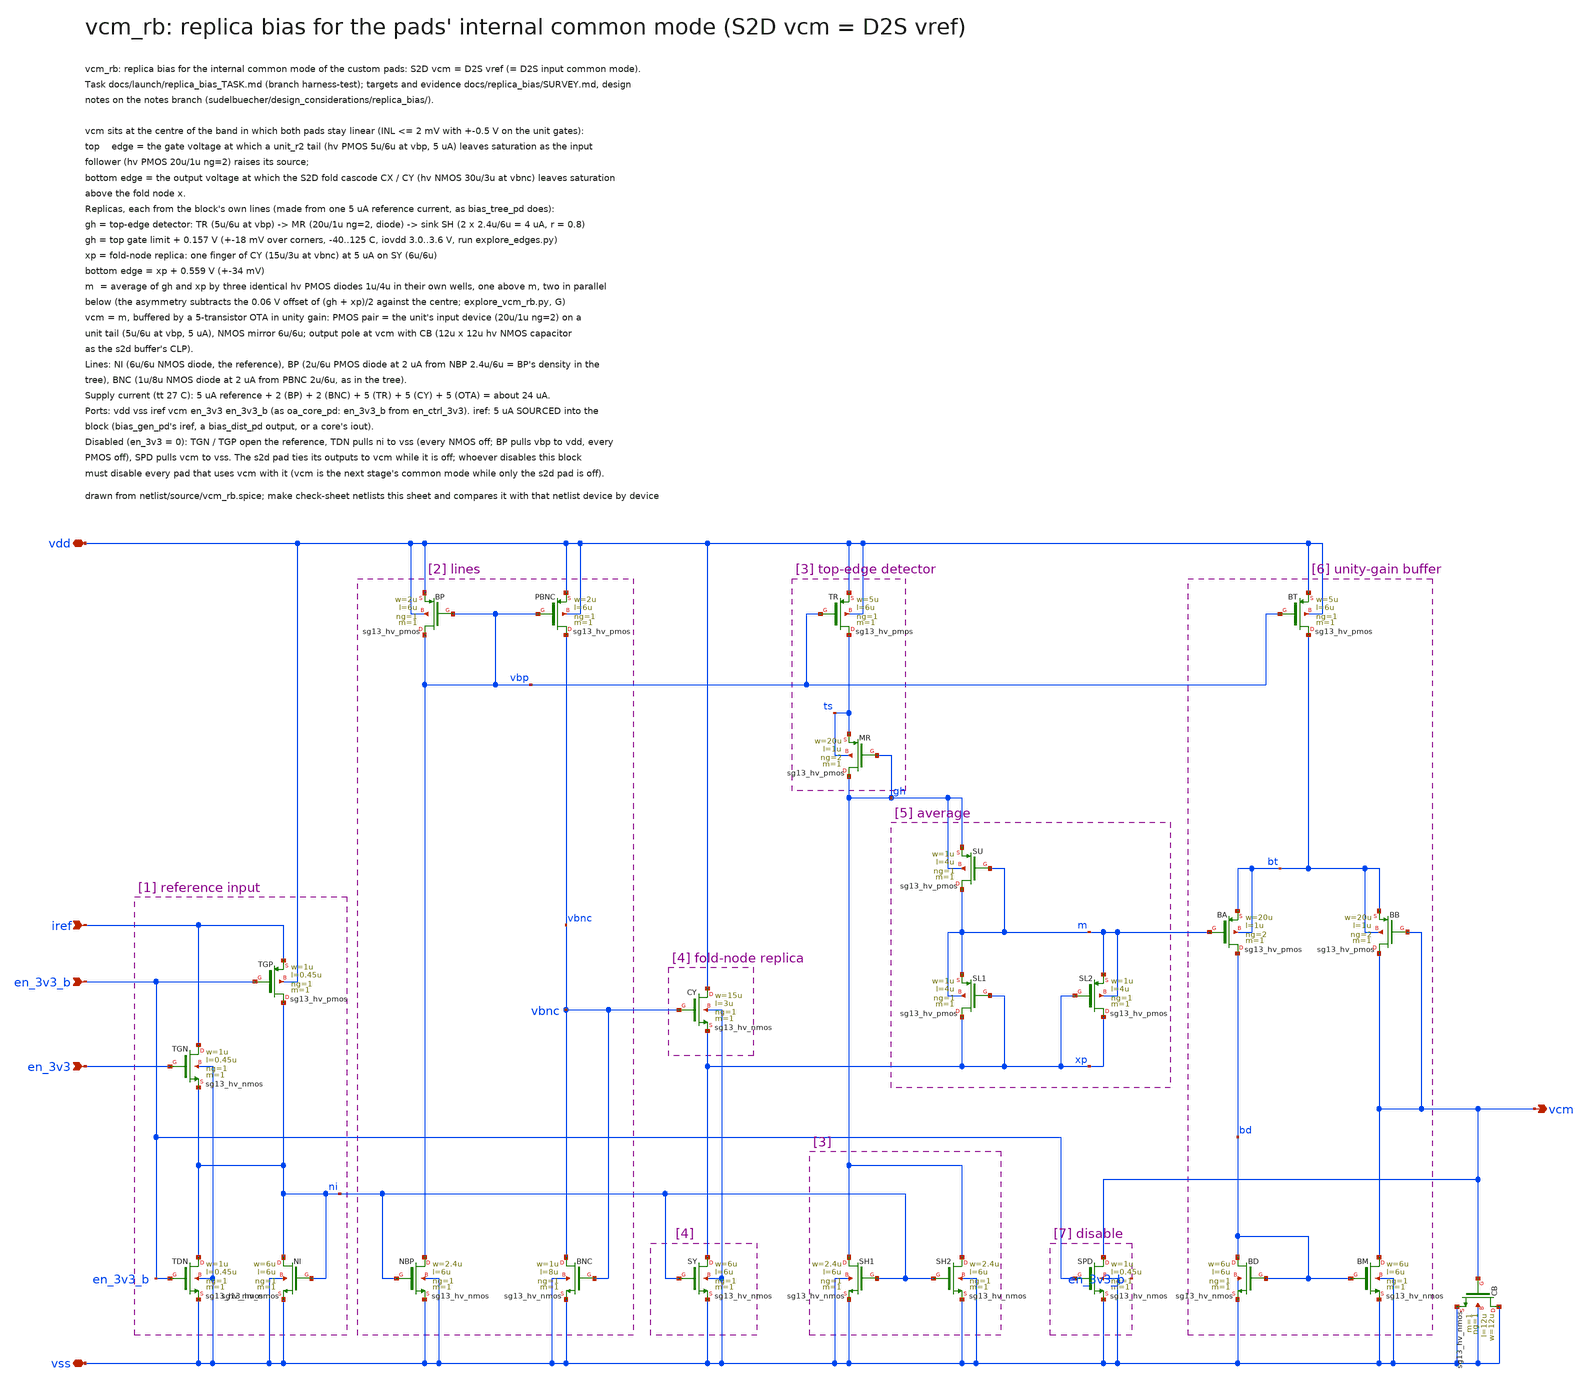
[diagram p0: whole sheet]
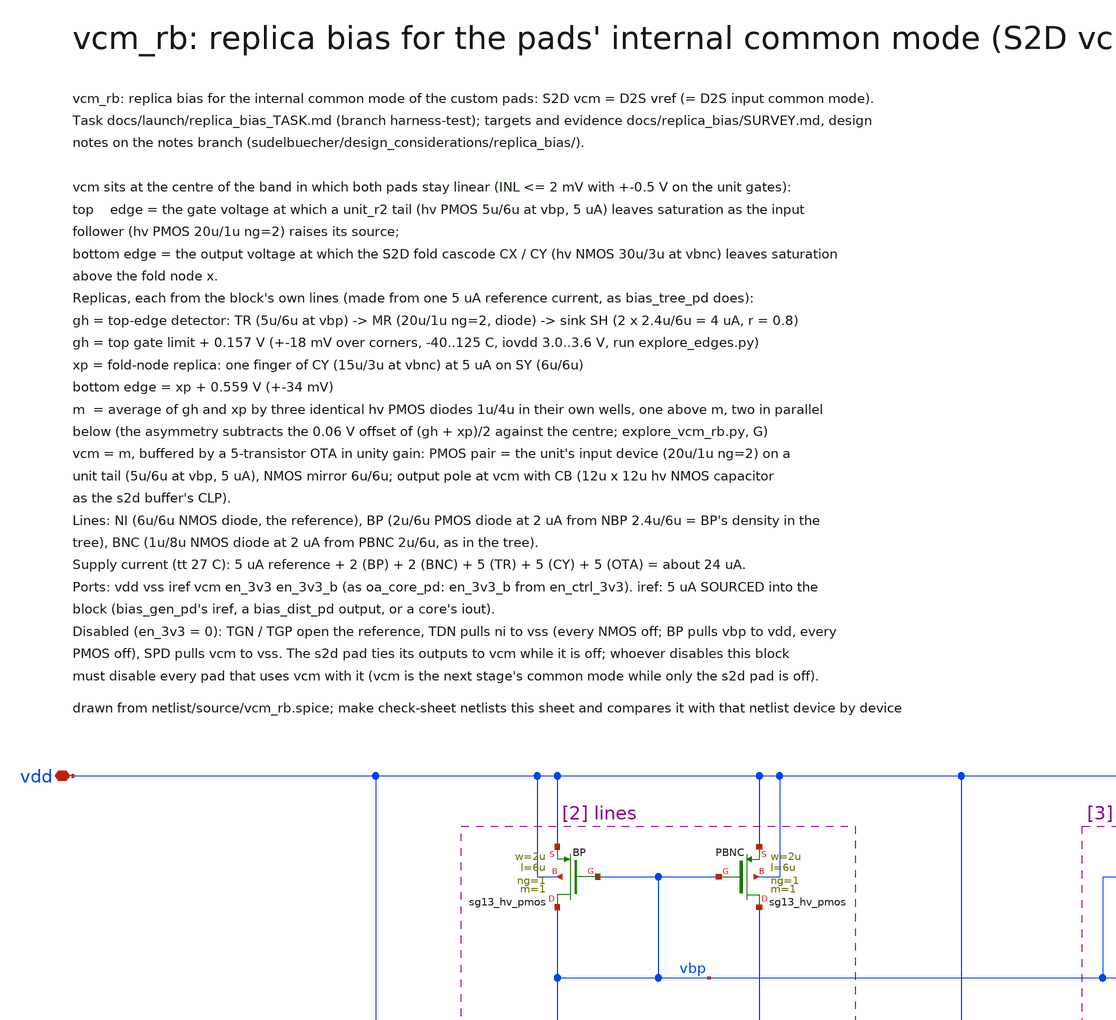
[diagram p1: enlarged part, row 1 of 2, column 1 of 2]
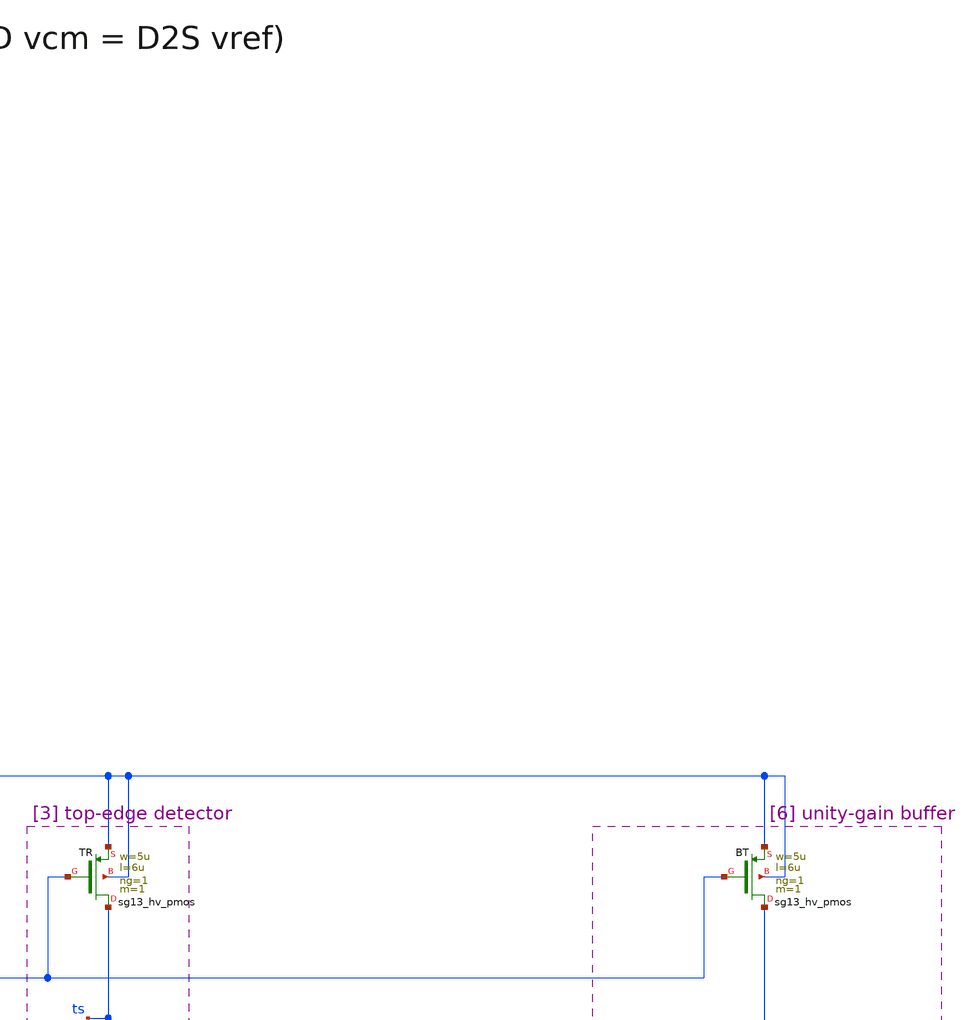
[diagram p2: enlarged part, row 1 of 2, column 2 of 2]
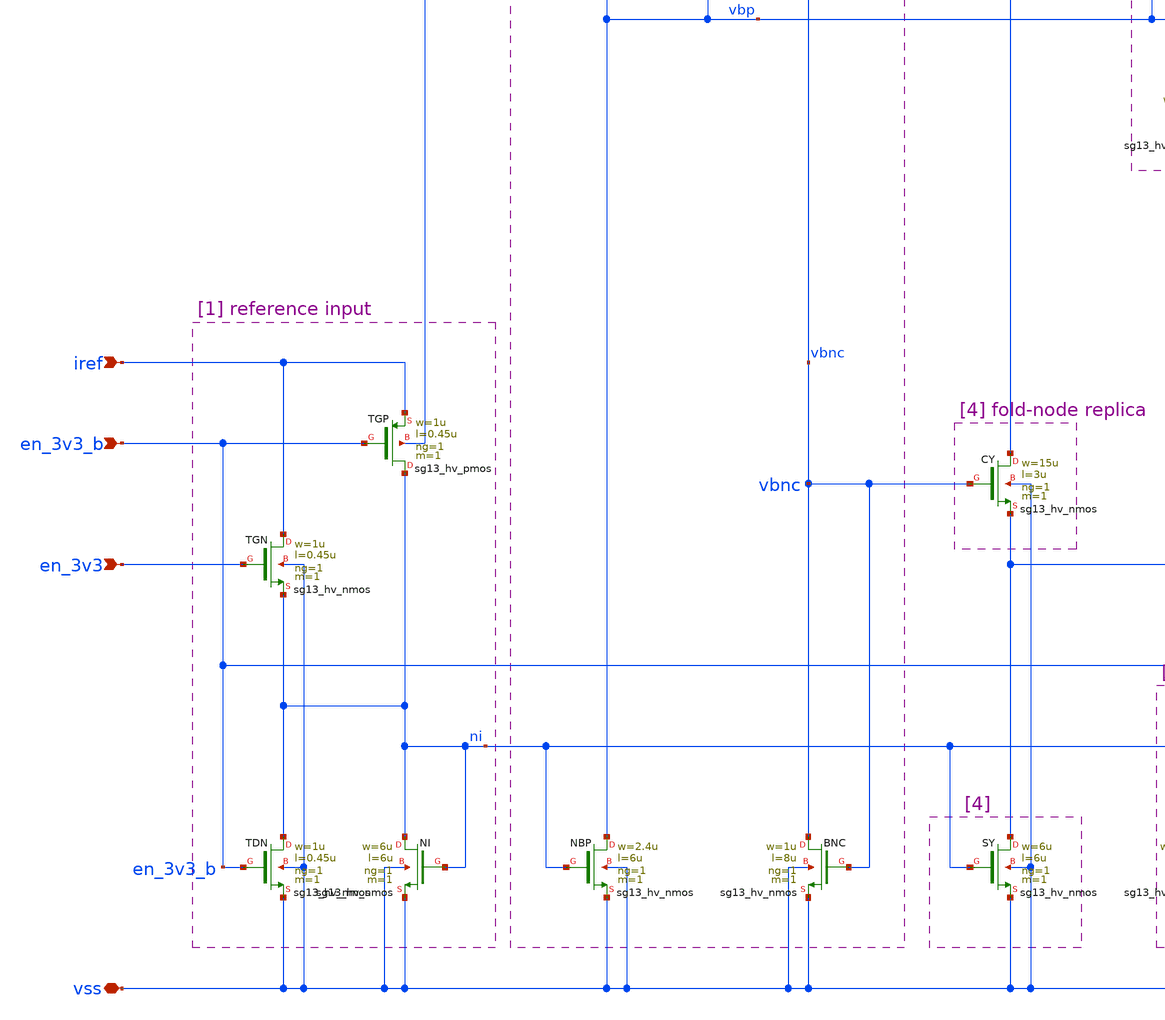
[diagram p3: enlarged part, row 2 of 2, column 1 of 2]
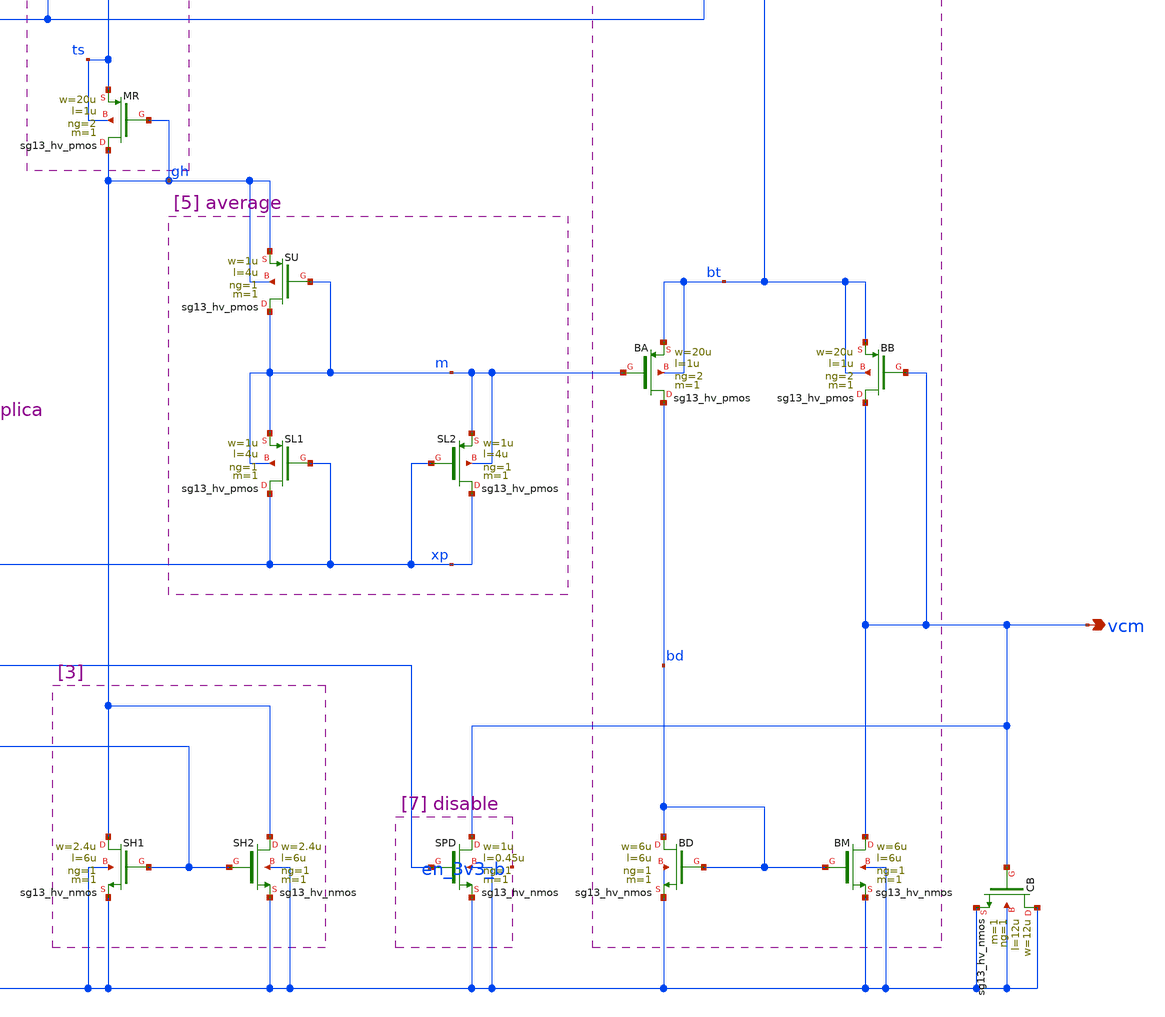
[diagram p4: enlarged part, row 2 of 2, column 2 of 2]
** sch_path: macros/vcm_rb/schematic/xschem/vcm_rb.sch
**.subckt vcm_rb vdd vss iref vcm en_3v3 en_3v3_b
*.iopin vdd
*.iopin vss
*.ipin iref
*.opin vcm
*.ipin en_3v3
*.ipin en_3v3_b
XTGN iref en_3v3 ni vss sg13_hv_nmos w=1u l=0.45u ng=1 m=1 mm_ok=1
XTGP ni en_3v3_b iref vdd sg13_hv_pmos w=1u l=0.45u ng=1 m=1 mm_ok=1
XTDN ni en_3v3_b vss vss sg13_hv_nmos w=1u l=0.45u ng=1 m=1 mm_ok=1
XNI ni ni vss vss sg13_hv_nmos w=6u l=6u ng=1 m=1 mm_ok=1
XNBP vbp ni vss vss sg13_hv_nmos w=2.4u l=6u ng=1 m=1 mm_ok=1
XBP vbp vbp vdd vdd sg13_hv_pmos w=2u l=6u ng=1 m=1 mm_ok=1
XPBNC vbnc vbp vdd vdd sg13_hv_pmos w=2u l=6u ng=1 m=1 mm_ok=1
XBNC vbnc vbnc vss vss sg13_hv_nmos w=1u l=8u ng=1 m=1 mm_ok=1
XTR ts vbp vdd vdd sg13_hv_pmos w=5u l=6u ng=1 m=1 mm_ok=1
XMR gh gh ts ts sg13_hv_pmos w=20u l=1u ng=2 m=1 mm_ok=1
XSH1 gh ni vss vss sg13_hv_nmos w=2.4u l=6u ng=1 m=1 mm_ok=1
XSH2 gh ni vss vss sg13_hv_nmos w=2.4u l=6u ng=1 m=1 mm_ok=1
XCY vdd vbnc xp vss sg13_hv_nmos w=15u l=3u ng=1 m=1 mm_ok=1
XSY xp ni vss vss sg13_hv_nmos w=6u l=6u ng=1 m=1 mm_ok=1
XSU m m gh gh sg13_hv_pmos w=1u l=4u ng=1 m=1 mm_ok=1
XSL1 xp xp m m sg13_hv_pmos w=1u l=4u ng=1 m=1 mm_ok=1
XSL2 xp xp m m sg13_hv_pmos w=1u l=4u ng=1 m=1 mm_ok=1
XBT bt vbp vdd vdd sg13_hv_pmos w=5u l=6u ng=1 m=1 mm_ok=1
XBA bd m bt bt sg13_hv_pmos w=20u l=1u ng=2 m=1 mm_ok=1
XBB vcm vcm bt bt sg13_hv_pmos w=20u l=1u ng=2 m=1 mm_ok=1
XBD bd bd vss vss sg13_hv_nmos w=6u l=6u ng=1 m=1 mm_ok=1
XBM vcm bd vss vss sg13_hv_nmos w=6u l=6u ng=1 m=1 mm_ok=1
XCB vss vcm vss vss sg13_hv_nmos w=12u l=12u ng=1 m=1 mm_ok=1
XSPD vcm en_3v3_b vss vss sg13_hv_nmos w=1u l=0.45u ng=1 m=1 mm_ok=1
**.ends
.end
